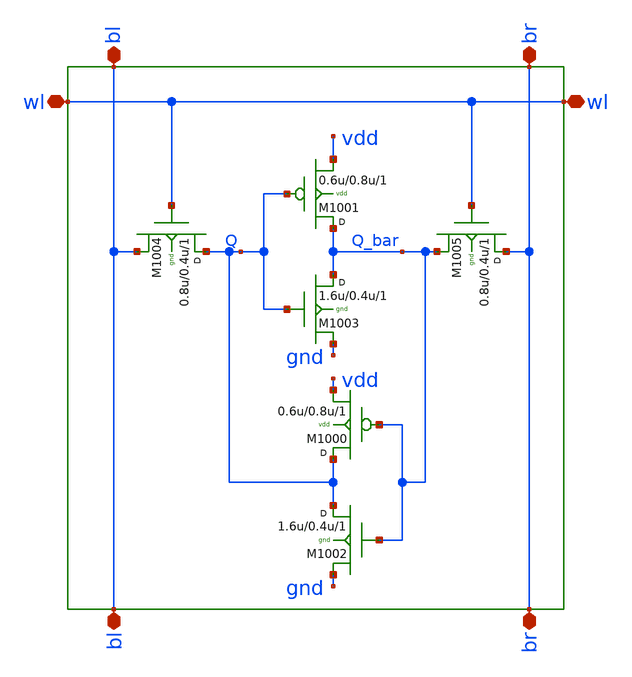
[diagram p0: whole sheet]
** sch_path: sram_2_64_scn4m_lcc/cell_1rw_passthru.sch
**.subckt cell_1rw_passthru bl br wl wl bl br
*.iopin bl
*.iopin br
*.iopin wl
*.iopin wl
*.iopin bl
*.iopin br
M1003 Q_bar Q gnd gnd n w=1.6u l=0.4u m=1
M1004 Q wl bl gnd n w=0.8u l=0.4u m=1
M1001 Q_bar Q vdd vdd p w=0.6u l=0.8u m=1
M1005 br wl Q_bar gnd n w=0.8u l=0.4u m=1
M1002 Q Q_bar gnd gnd n w=1.6u l=0.4u m=1
M1000 Q Q_bar vdd vdd p w=0.6u l=0.8u m=1
**.ends
.end
